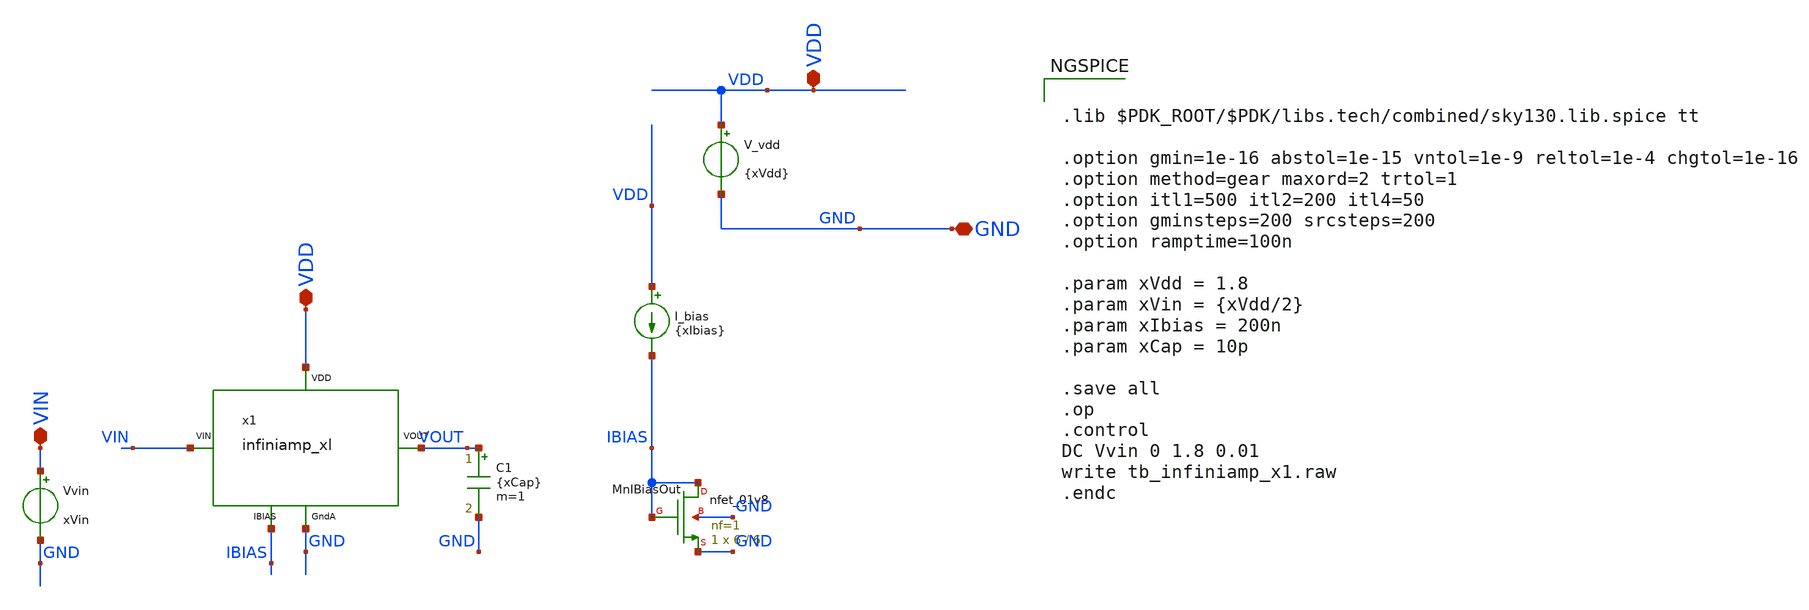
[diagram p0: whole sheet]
** sch_path: analog/xschem/tb_infiniamp_x1.sch
**.subckt tb_infiniamp_x1 VDD GND VIN VDD
*.iopin VDD
*.iopin GND
*.iopin VIN
*.iopin VDD
x1 VDD VIN VOUT IBIAS GND infiniamp_xl
V_vdd VDD GND {xVdd}
Vvin VIN GND xVin
I_bias VDD IBIAS {xIbias}
C1 VOUT GND {xCap} m=1
XMnIBiasOut IBIAS IBIAS GND GND sky130_fd_pr__nfet_01v8 L=6 W=6 nf=1 ad='int((1 + 1)/2) * 6 / 1 * 0.29'
+ as='int((1 + 2)/2) * 6 / 1 * 0.29' pd='2*int((1 + 1)/2) * (6 / 1 + 0.29)' ps='2*int((1 + 2)/2) * (6 / 1 + 0.29)'
+ nrd='0.29 / 6 ' nrs='0.29 / 6 ' sa=0 sb=0 sd=0 mult=1 m=1
**** begin user architecture code


.lib $PDK_ROOT/$PDK/libs.tech/combined/sky130.lib.spice tt

.option gmin=1e-16 abstol=1e-15 vntol=1e-9 reltol=1e-4 chgtol=1e-16
.option method=gear maxord=2 trtol=1
.option itl1=500 itl2=200 itl4=50
.option gminsteps=200 srcsteps=200
.option ramptime=100n

.param xVdd = 1.8
.param xVin = {xVdd/2}
.param xIbias = 200n
.param xCap = 10p

.save all
.op
.control
DC Vvin 0 1.8 0.01
write tb_infiniamp_x1.raw
.endc


**** end user architecture code
**.ends

* expanding   symbol:  infiniamp_xl.sym # of pins=5
** sym_path: analog/xschem/infiniamp_xl.sym
** sch_path: analog/xschem/infiniamp_xl.sch
.subckt infiniamp_xl VDD VIN VOUT IBIAS GndA
*.iopin VDD
*.iopin GndA
*.ipin VIN
*.iopin IBIAS
*.iopin VOUT
XMpBiasIn VBIAS_P VBIAS_P VDD VDD sky130_fd_pr__pfet_01v8 L=0.4 W=1 nf=1 ad='int((1 + 1)/2) * 1 / 1 * 0.29'
+ as='int((1 + 2)/2) * 1 / 1 * 0.29' pd='2*int((1 + 1)/2) * (1 / 1 + 0.29)' ps='2*int((1 + 2)/2) * (1 / 1 + 0.29)'
+ nrd='0.29 / 1 ' nrs='0.29 / 1 ' sa=0 sb=0 sd=0 mult=4 m=4
XMpAuxBias AUX_SOURCE VBIAS_P VDD VDD sky130_fd_pr__pfet_01v8 L=0.4 W=1 nf=1 ad='int((1 + 1)/2) * 1 / 1 * 0.29'
+ as='int((1 + 2)/2) * 1 / 1 * 0.29' pd='2*int((1 + 1)/2) * (1 / 1 + 0.29)' ps='2*int((1 + 2)/2) * (1 / 1 + 0.29)'
+ nrd='0.29 / 1 ' nrs='0.29 / 1 ' sa=0 sb=0 sd=0 mult=4 m=4
XMpSrcBias MAIN_SOURCE VBIAS_P VDD VDD sky130_fd_pr__pfet_01v8 L=0.4 W=1 nf=1 ad='int((1 + 1)/2) * 1 / 1 * 0.29'
+ as='int((1 + 2)/2) * 1 / 1 * 0.29' pd='2*int((1 + 1)/2) * (1 / 1 + 0.29)' ps='2*int((1 + 2)/2) * (1 / 1 + 0.29)'
+ nrd='0.29 / 1 ' nrs='0.29 / 1 ' sa=0 sb=0 sd=0 mult=16 m=16
XMpAuxNVin DIODE_LD N_VIN AUX_SOURCE AUX_SOURCE sky130_fd_pr__pfet_01v8_lvt L=0.4 W=6 nf=1 ad='int((1 + 1)/2) * 6 / 1 * 0.29'
+ as='int((1 + 2)/2) * 6 / 1 * 0.29' pd='2*int((1 + 1)/2) * (6 / 1 + 0.29)' ps='2*int((1 + 2)/2) * (6 / 1 + 0.29)'
+ nrd='0.29 / 6 ' nrs='0.29 / 6 ' sa=0 sb=0 sd=0 mult=8 m=8
XMpAuxVout MAIN_BIAS VOUT AUX_SOURCE AUX_SOURCE sky130_fd_pr__pfet_01v8_lvt L=0.4 W=6 nf=1 ad='int((1 + 1)/2) * 6 / 1 * 0.29'
+ as='int((1 + 2)/2) * 6 / 1 * 0.29' pd='2*int((1 + 1)/2) * (6 / 1 + 0.29)' ps='2*int((1 + 2)/2) * (6 / 1 + 0.29)'
+ nrd='0.29 / 6 ' nrs='0.29 / 6 ' sa=0 sb=0 sd=0 mult=8 m=8
XMpSrcVin N_VIN VIN MAIN_SOURCE MAIN_SOURCE sky130_fd_pr__pfet_01v8_lvt L=0.4 W=6 nf=1 ad='int((1 + 1)/2) * 6 / 1 * 0.29'
+ as='int((1 + 2)/2) * 6 / 1 * 0.29' pd='2*int((1 + 1)/2) * (6 / 1 + 0.29)' ps='2*int((1 + 2)/2) * (6 / 1 + 0.29)'
+ nrd='0.29 / 6 ' nrs='0.29 / 6 ' sa=0 sb=0 sd=0 mult=8 m=8
XMpSrcVout VOUT VOUT MAIN_SOURCE MAIN_SOURCE sky130_fd_pr__pfet_01v8_lvt L=0.4 W=6 nf=1 ad='int((1 + 1)/2) * 6 / 1 * 0.29'
+ as='int((1 + 2)/2) * 6 / 1 * 0.29' pd='2*int((1 + 1)/2) * (6 / 1 + 0.29)' ps='2*int((1 + 2)/2) * (6 / 1 + 0.29)'
+ nrd='0.29 / 6 ' nrs='0.29 / 6 ' sa=0 sb=0 sd=0 mult=8 m=8
XMnBiasIn VBIAS_P IBIAS GndA GndA sky130_fd_pr__nfet_01v8 L=6 W=15 nf=1 ad='int((1 + 1)/2) * 15 / 1 * 0.29'
+ as='int((1 + 2)/2) * 15 / 1 * 0.29' pd='2*int((1 + 1)/2) * (15 / 1 + 0.29)' ps='2*int((1 + 2)/2) * (15 / 1 + 0.29)'
+ nrd='0.29 / 15 ' nrs='0.29 / 15 ' sa=0 sb=0 sd=0 mult=5 m=5
XMnDiodeLD DIODE_LD DIODE_LD GndA GndA sky130_fd_pr__nfet_01v8 L=0.4 W=2 nf=1 ad='int((1 + 1)/2) * 2 / 1 * 0.29'
+ as='int((1 + 2)/2) * 2 / 1 * 0.29' pd='2*int((1 + 1)/2) * (2 / 1 + 0.29)' ps='2*int((1 + 2)/2) * (2 / 1 + 0.29)'
+ nrd='0.29 / 2 ' nrs='0.29 / 2 ' sa=0 sb=0 sd=0 mult=2 m=2
XMnMainBias MAIN_BIAS MAIN_BIAS GndA GndA sky130_fd_pr__nfet_01v8 L=0.4 W=2 nf=1 ad='int((1 + 1)/2) * 2 / 1 * 0.29'
+ as='int((1 + 2)/2) * 2 / 1 * 0.29' pd='2*int((1 + 1)/2) * (2 / 1 + 0.29)' ps='2*int((1 + 2)/2) * (2 / 1 + 0.29)'
+ nrd='0.29 / 2 ' nrs='0.29 / 2 ' sa=0 sb=0 sd=0 mult=2 m=2
XMnNVin N_VIN MAIN_BIAS GndA GndA sky130_fd_pr__nfet_01v8 L=0.4 W=2 nf=1 ad='int((1 + 1)/2) * 2 / 1 * 0.29'
+ as='int((1 + 2)/2) * 2 / 1 * 0.29' pd='2*int((1 + 1)/2) * (2 / 1 + 0.29)' ps='2*int((1 + 2)/2) * (2 / 1 + 0.29)'
+ nrd='0.29 / 2 ' nrs='0.29 / 2 ' sa=0 sb=0 sd=0 mult=8 m=8
XMnVout VOUT MAIN_BIAS GndA GndA sky130_fd_pr__nfet_01v8 L=0.4 W=2 nf=1 ad='int((1 + 1)/2) * 2 / 1 * 0.29'
+ as='int((1 + 2)/2) * 2 / 1 * 0.29' pd='2*int((1 + 1)/2) * (2 / 1 + 0.29)' ps='2*int((1 + 2)/2) * (2 / 1 + 0.29)'
+ nrd='0.29 / 2 ' nrs='0.29 / 2 ' sa=0 sb=0 sd=0 mult=8 m=8
.ends

.end
